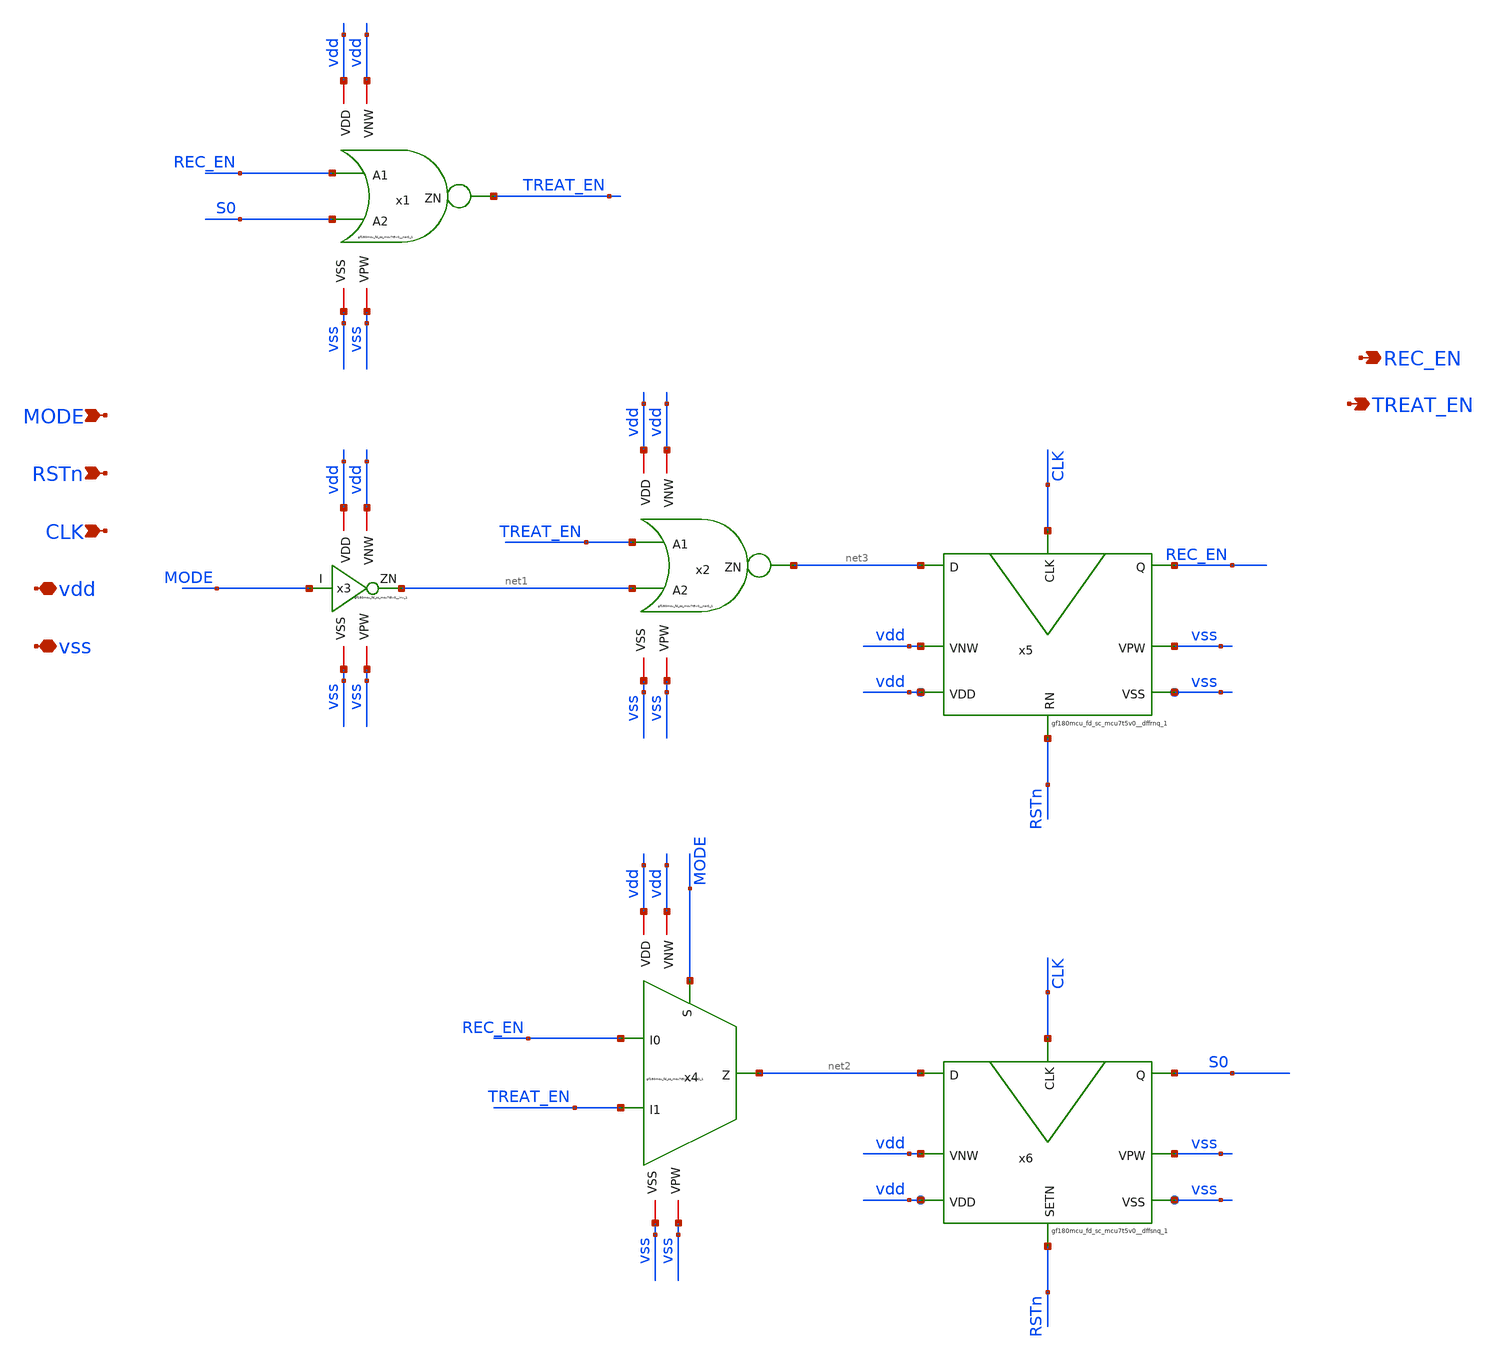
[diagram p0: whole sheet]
** sch_path: FSM.sch
**.subckt FSM REC_EN MODE RSTn CLK TREAT_EN vdd vss
*.opin REC_EN
*.ipin MODE
*.ipin RSTn
*.ipin CLK
*.opin TREAT_EN
*.iopin vdd
*.iopin vss
x1 REC_EN S0 TREAT_EN vdd vdd vss vss gf180mcu_fd_sc_mcu7t5v0__nor2_1
x2 TREAT_EN net1 net3 vdd vdd vss vss gf180mcu_fd_sc_mcu7t5v0__nor2_1
x3 MODE net1 vdd vdd vss vss gf180mcu_fd_sc_mcu7t5v0__inv_1
x4 REC_EN TREAT_EN MODE net2 vdd vdd vss vss gf180mcu_fd_sc_mcu7t5v0__mux2_1
x5 net3 RSTn CLK REC_EN vdd vdd vss vss gf180mcu_fd_sc_mcu7t5v0__dffrnq_1
x6 net2 RSTn CLK S0 vdd vdd vss vss gf180mcu_fd_sc_mcu7t5v0__dffsnq_1
**.ends
.end
